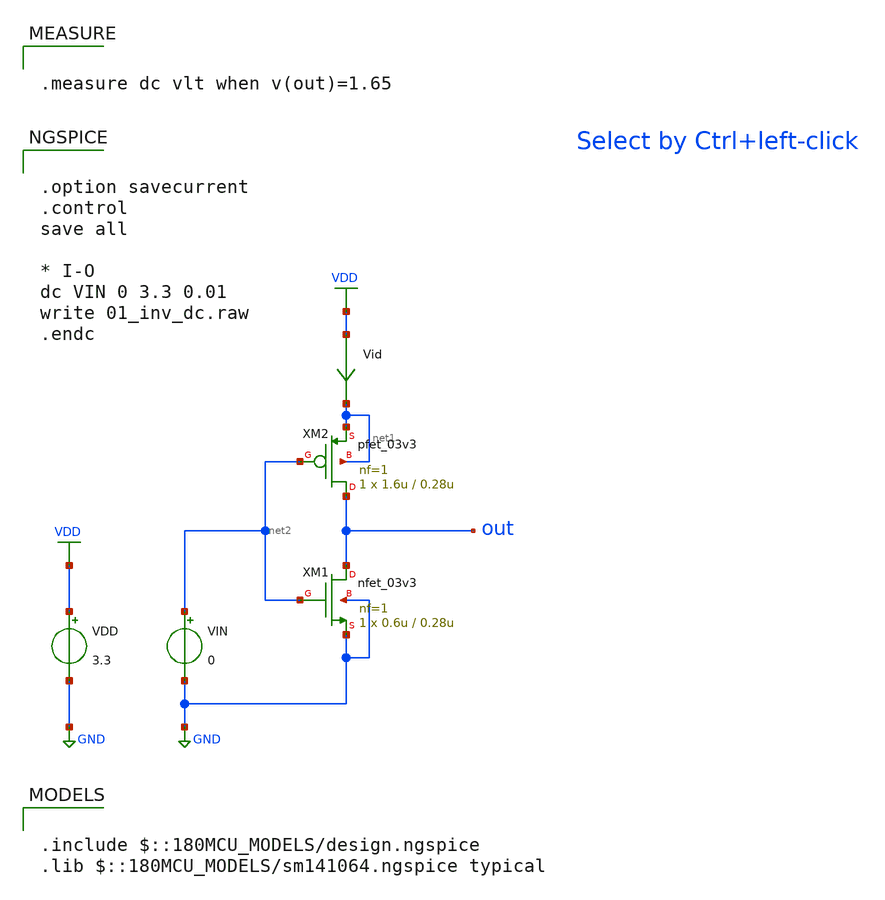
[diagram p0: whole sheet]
** sch_path: fifty_nifty/01_inv_dc.sch
**.subckt 01_inv_dc
XM1 out net2 GND GND nfet_03v3 L=0.28u W=0.6u nf=1 ad='int((nf+1)/2) * W/nf * 0.18u' as='int((nf+2)/2) * W/nf * 0.18u'
+ pd='2*int((nf+1)/2) * (W/nf + 0.18u)' ps='2*int((nf+2)/2) * (W/nf + 0.18u)' nrd='0.18u / W' nrs='0.18u / W'
+ sa=0 sb=0 sd=0 m=1
VIN net2 GND 0
Vid VDD net1 0
.save i(vid)
XM2 out net2 net1 net1 pfet_03v3 L=0.28u W=1.6u nf=1 ad='int((nf+1)/2) * W/nf * 0.18u' as='int((nf+2)/2) * W/nf * 0.18u'
+ pd='2*int((nf+1)/2) * (W/nf + 0.18u)' ps='2*int((nf+2)/2) * (W/nf + 0.18u)' nrd='0.18u / W' nrs='0.18u / W'
+ sa=0 sb=0 sd=0 m=1
VDD VDD GND 3.3
**** begin user architecture code

.option savecurrent
.control
save all

* I-O
dc VIN 0 3.3 0.01
write 01_inv_dc.raw
.endc


.include $::180MCU_MODELS/design.ngspice
.lib $::180MCU_MODELS/sm141064.ngspice typical


.measure dc vlt when v(out)=1.65

**** end user architecture code
**.ends
.GLOBAL GND
.GLOBAL VDD
.end
